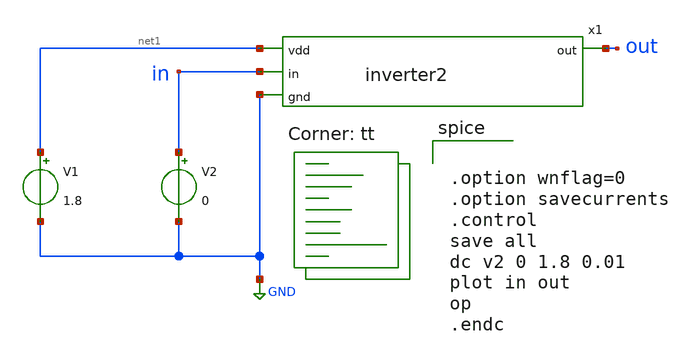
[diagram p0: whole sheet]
** sch_path: icdec_inverter2/inverter2_tb.sch
**.subckt inverter2_tb
x1 net1 in out GND inverter2
V1 net1 GND 1.8
V2 in GND 0
**** begin user architecture code

** opencircuitdesign pdks install
.lib $::SKYWATER_MODELS/sky130.lib.spice tt




.option wnflag=0
.option savecurrents
.control
save all
dc v2 0 1.8 0.01
plot in out
op
.endc


**** end user architecture code
**.ends

* expanding   symbol:  inverter2.sym # of pins=4
** sym_path: icdec_inverter2/inverter2.sym
** sch_path: icdec_inverter2/inverter2.sch
.subckt inverter2 vdd in out gnd
*.opin out
*.ipin vdd
*.ipin in
*.ipin gnd
XM1 out in gnd gnd sky130_fd_pr__nfet_01v8 L=0.15 W=1 nf=1 ad='int((nf+1)/2) * W/nf * 0.29' as='int((nf+2)/2) * W/nf * 0.29'
+ pd='2*int((nf+1)/2) * (W/nf + 0.29)' ps='2*int((nf+2)/2) * (W/nf + 0.29)' nrd='0.29 / W' nrs='0.29 / W'
+ sa=0 sb=0 sd=0 mult=1 m=1
XM2 out in vdd vdd sky130_fd_pr__pfet_01v8 L=0.15 W=1 nf=1 ad='int((nf+1)/2) * W/nf * 0.29' as='int((nf+2)/2) * W/nf * 0.29'
+ pd='2*int((nf+1)/2) * (W/nf + 0.29)' ps='2*int((nf+2)/2) * (W/nf + 0.29)' nrd='0.29 / W' nrs='0.29 / W'
+ sa=0 sb=0 sd=0 mult=1 m=1
.ends

.GLOBAL GND
.end
